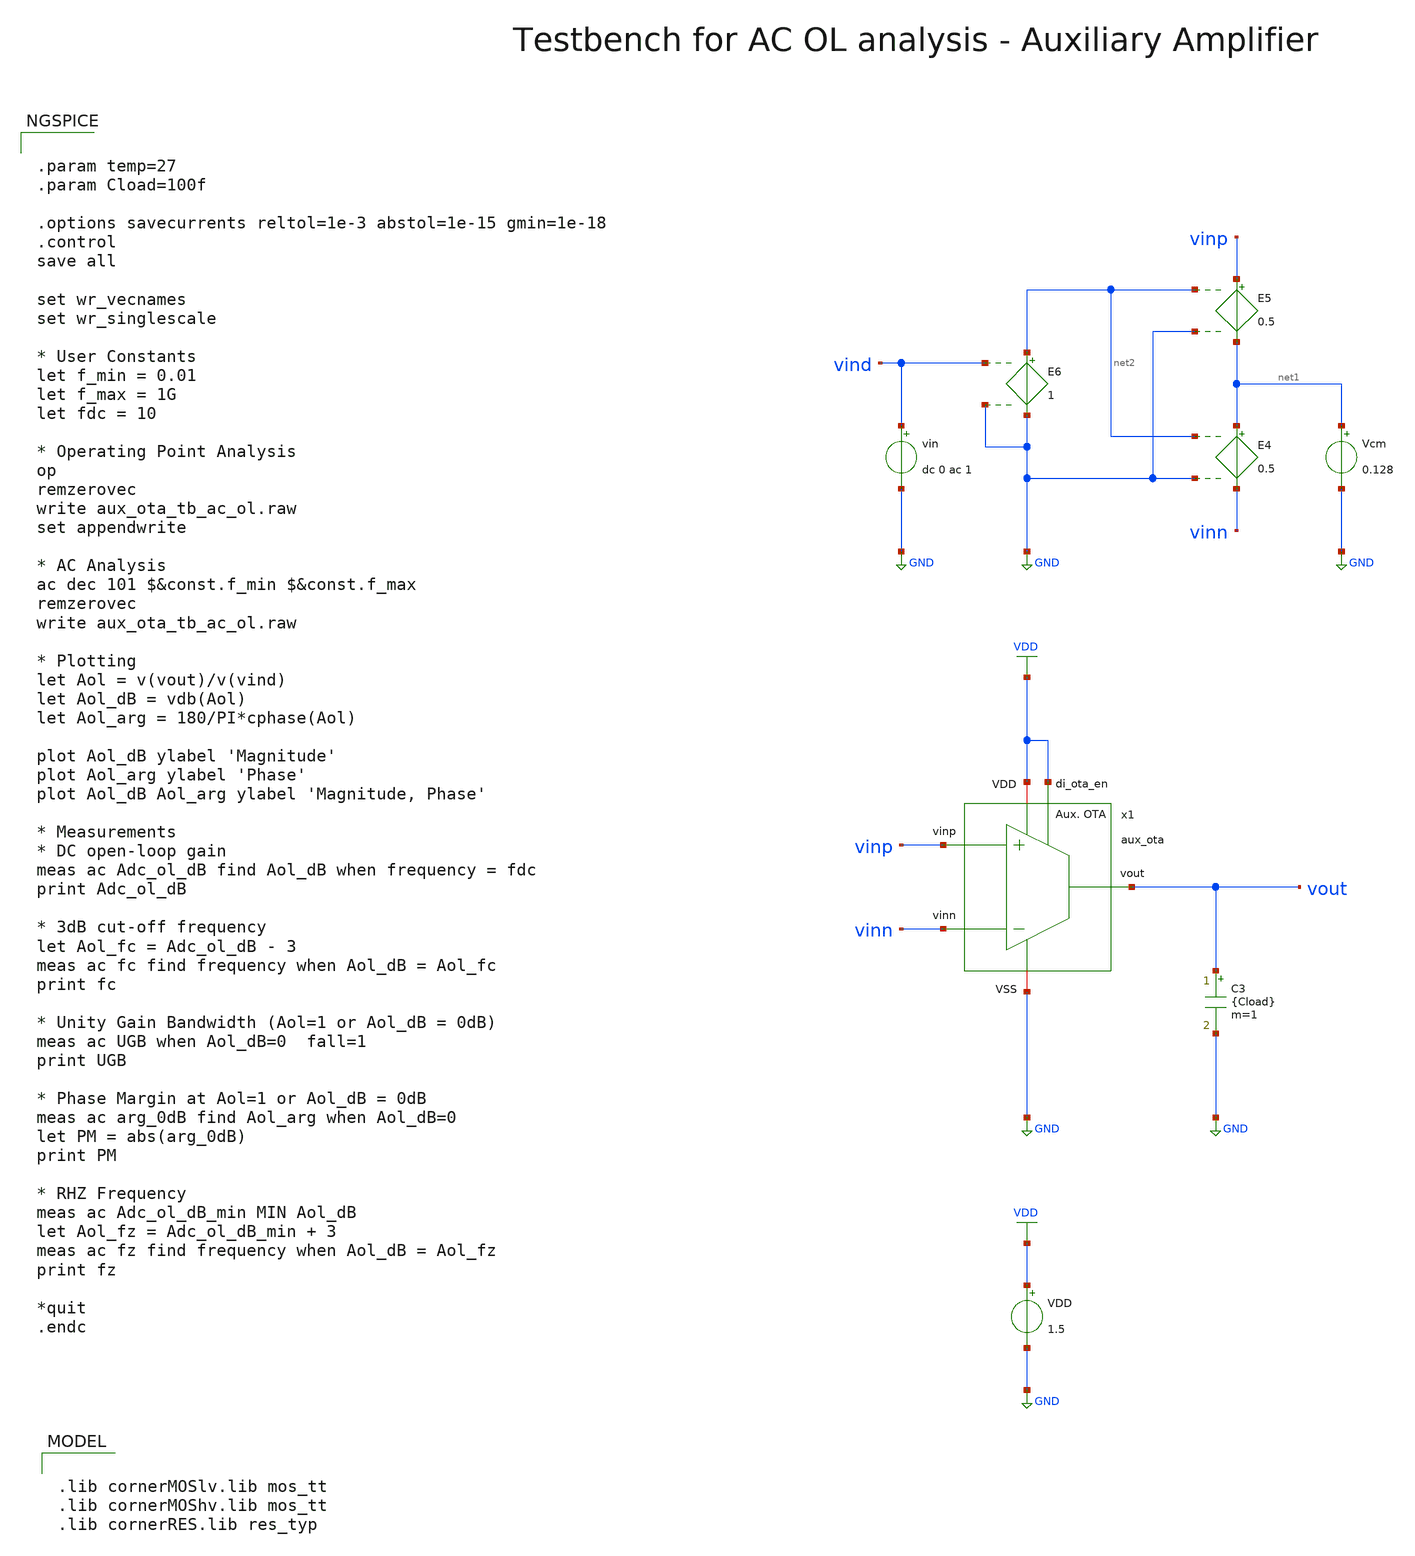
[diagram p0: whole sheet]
** sch_path: SG13G2_ATBS-ADC-main/xschem/bio_amplifier/amplifier_core/bias_circuit/aux_ota/testbenches/aux_ota_tb_ac_ol.sch
**.subckt aux_ota_tb_ac_ol
VDD VDD GND 1.5
Vcm net1 GND 0.128
E4 net1 vinn net2 GND 0.5
E5 vinp net1 net2 GND 0.5
E6 net2 GND vind GND 1
vin vind GND dc 0 ac 1
C3 vout GND {Cload} m=1
x1 VDD vout vinn vinp VDD GND aux_ota
**** begin user architecture code


.param temp=27
.param Cload=100f

.options savecurrents reltol=1e-3 abstol=1e-15 gmin=1e-18
.control
save all

set wr_vecnames
set wr_singlescale

* User Constants
let f_min = 0.01
let f_max = 1G
let fdc = 10

* Operating Point Analysis
op
remzerovec
write aux_ota_tb_ac_ol.raw
set appendwrite

* AC Analysis
ac dec 101 $&const.f_min $&const.f_max
remzerovec
write aux_ota_tb_ac_ol.raw

* Plotting
let Aol = v(vout)/v(vind)
let Aol_dB = vdb(Aol)
let Aol_arg = 180/PI*cphase(Aol)

plot Aol_dB ylabel 'Magnitude'
plot Aol_arg ylabel 'Phase'
plot Aol_dB Aol_arg ylabel 'Magnitude, Phase'

* Measurements
* DC open-loop gain
meas ac Adc_ol_dB find Aol_dB when frequency = fdc
print Adc_ol_dB

* 3dB cut-off frequency
let Aol_fc = Adc_ol_dB - 3
meas ac fc find frequency when Aol_dB = Aol_fc
print fc

* Unity Gain Bandwidth (Aol=1 or Aol_dB = 0dB)
meas ac UGB when Aol_dB=0  fall=1
print UGB

* Phase Margin at Aol=1 or Aol_dB = 0dB
meas ac arg_0dB find Aol_arg when Aol_dB=0
let PM = abs(arg_0dB)
print PM

* RHZ Frequency
meas ac Adc_ol_dB_min MIN Aol_dB
let Aol_fz = Adc_ol_dB_min + 3
meas ac fz find frequency when Aol_dB = Aol_fz
print fz

*quit
.endc



.lib cornerMOSlv.lib mos_tt
.lib cornerMOShv.lib mos_tt
.lib cornerRES.lib res_typ

**** end user architecture code
**.ends

* expanding   symbol:  bio_amplifier/amplifier_core/bias_circuit/aux_ota/aux_ota.sym # of pins=6
** sym_path: SG13G2_ATBS-ADC-main/xschem/bio_amplifier/amplifier_core/bias_circuit/aux_ota/aux_ota.sym
** sch_path: SG13G2_ATBS-ADC-main/xschem/bio_amplifier/amplifier_core/bias_circuit/aux_ota/aux_ota.sch
.subckt aux_ota di_ota_en vout vinn vinp VDD VSS
*.iopin VDD
*.iopin VSS
*.ipin di_ota_en
*.ipin vinp
*.ipin vinn
*.opin vout
xM3 net1 Vgs_ma34 net2 net2 sg13g2_lv_pmos_stacked_x4 W_P=20.0u L_P=40.0u NG_P=20 M_P=1
xM4 vout Vgs_ma34 net2 net2 sg13g2_lv_pmos_stacked_x4 W_P=20.0u L_P=40.0u NG_P=20 M_P=1
xM1 net1 vinp VSS VSS sg13g2_lv_nmos_stacked_x2 W_N=5.0u L_N=40.0u NG_N=5 M_N=1
VIdd VDD net2 0
.save i(vidd)
xM2 vout vinn VSS VSS sg13g2_lv_nmos_stacked_x2 W_N=5.0u L_N=40.0u NG_N=5 M_N=1
XMPD1 Vgs_ma34 di_ota_en net2 net2 sg13_lv_pmos w=1.0u l=0.13u ng=1 m=1 mm_ok=1
XMPD2 net1 ota_en_n Vgs_ma34 net2 sg13_lv_pmos w=1.0u l=0.13u ng=1 m=1 mm_ok=1
x1 VDD di_ota_en ota_en_n VSS inverter_lv W_P=1.0u L_P=0.13u W_N=1.0u L_N=0.13u
.ends


* expanding   symbol:  stacked_transistors/sg13g2_lv_pmos_stacked/sg13g2_lv_pmos_stacked_x4.sym # of
*+ pins=4
** sym_path: SG13G2_ATBS-ADC-main/xschem/stacked_transistors/sg13g2_lv_pmos_stacked/sg13g2_lv_pmos_stacked_x4.sym
** sch_path: SG13G2_ATBS-ADC-main/xschem/stacked_transistors/sg13g2_lv_pmos_stacked/sg13g2_lv_pmos_stacked_x4.sch
.subckt sg13g2_lv_pmos_stacked_x4 D G B S  W_P=1.0u L_P=0.45u NG_P=1 M_P=1
*.iopin D
*.iopin S
*.iopin G
*.iopin B
XM1 net1 G S B sg13_lv_pmos w=W_P l=L_P/4 ng=NG_P m=M_P mm_ok=1
XM2 net3 G net1 B sg13_lv_pmos w=W_P l=L_P/4 ng=NG_P m=M_P mm_ok=1
XM3 net2 G net3 B sg13_lv_pmos w=W_P l=L_P/4 ng=NG_P m=M_P mm_ok=1
XM4 D G net2 B sg13_lv_pmos w=W_P l=L_P/4 ng=NG_P m=M_P mm_ok=1
.ends


* expanding   symbol:  stacked_transistors/sg13g2_lv_nmos_stacked/sg13g2_lv_nmos_stacked_x2.sym # of
*+ pins=4
** sym_path: SG13G2_ATBS-ADC-main/xschem/stacked_transistors/sg13g2_lv_nmos_stacked/sg13g2_lv_nmos_stacked_x2.sym
** sch_path: SG13G2_ATBS-ADC-main/xschem/stacked_transistors/sg13g2_lv_nmos_stacked/sg13g2_lv_nmos_stacked_x2.sch
.subckt sg13g2_lv_nmos_stacked_x2 D G B S  W_N=1.0u L_N=0.45u NG_N=1 M_N=1
*.iopin D
*.iopin S
*.iopin G
*.iopin B
XM1 net1 G S B sg13_lv_nmos w=W_N l=L_N/2 ng=NG_N m=M_N mm_ok=1
XM2 D G net1 B sg13_lv_nmos w=W_N l=L_N/2 ng=NG_N m=M_N mm_ok=1
.ends


* expanding   symbol:  inverter/inverter_lv.sym # of pins=4
** sym_path: SG13G2_ATBS-ADC-main/xschem/inverter/inverter_lv.sym
** sch_path: SG13G2_ATBS-ADC-main/xschem/inverter/inverter_lv.sch
.subckt inverter_lv VDD vin vout VSS  W_P=3.0u L_P=0.13u W_N=1.0u L_N=0.13u
*.ipin vin
*.iopin VDD
*.iopin VSS
*.opin vout
XM1 vout vin VDD VDD sg13_lv_pmos w=W_P l=L_P ng=1 m=1 mm_ok=1
XM2 vout vin VSS VSS sg13_lv_nmos w=W_N l=L_N ng=1 m=1 mm_ok=1
.ends

.GLOBAL GND
.GLOBAL VDD
.end
